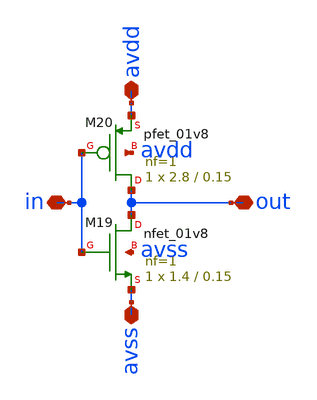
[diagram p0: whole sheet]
** sch_path: xschem/inv_simple1.sch
**.subckt inv_simple1 in avdd avss out
*.iopin in
*.iopin avdd
*.iopin avss
*.iopin out
XM19 out in avss avss sky130_fd_pr__nfet_01v8 L=0.15 W=1.4 nf=1 ad='int((nf+1)/2) * W/nf * 0.29' as='int((nf+2)/2) * W/nf * 0.29'
+ pd='2*int((nf+1)/2) * (W/nf + 0.29)' ps='2*int((nf+2)/2) * (W/nf + 0.29)' nrd='0.29 / W' nrs='0.29 / W'
+ sa=0 sb=0 sd=0 mult=1 m=1
XM20 out in avdd avdd sky130_fd_pr__pfet_01v8 L=0.15 W=2.8 nf=1 ad='int((nf+1)/2) * W/nf * 0.29' as='int((nf+2)/2) * W/nf * 0.29'
+ pd='2*int((nf+1)/2) * (W/nf + 0.29)' ps='2*int((nf+2)/2) * (W/nf + 0.29)' nrd='0.29 / W' nrs='0.29 / W'
+ sa=0 sb=0 sd=0 mult=1 m=1
**.ends
.end
